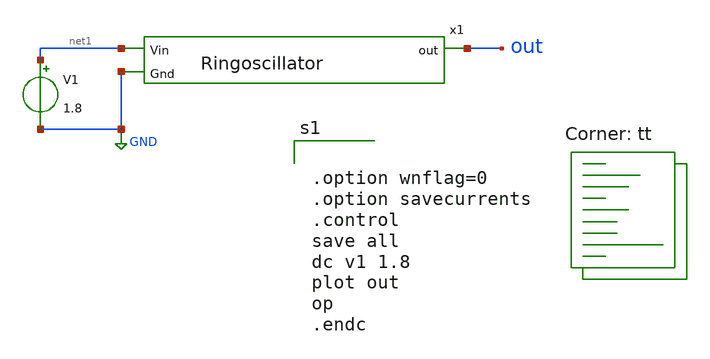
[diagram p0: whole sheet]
** sch_path: Inverter-Ringoscillator/RIngoscillator_simulation.sch
**.subckt RIngoscillator_simulation
x1 net1 out GND Ringoscillator
V1 net1 GND 1.8
**** begin user architecture code


.option wnflag=0
.option savecurrents
.control
save all
dc v1 1.8
plot out
op
.endc


.lib $::SKYWATER_MODELS/sky130.lib.spice tt
**** end user architecture code
**.ends

* expanding   symbol:  Ringoscillator.sym # of pins=3
** sym_path: Inverter-Ringoscillator/Ringoscillator.sym
** sch_path: Inverter-Ringoscillator/Ringoscillator.sch
.subckt Ringoscillator Vin out Gnd
*.opin out
*.ipin Vin
*.ipin Gnd
x1 Vin out net1 Gnd inverter
x2 Vin net1 net2 Gnd inverter
x3 Vin net2 out Gnd inverter
.ends


* expanding   symbol:  inverter.sym # of pins=4
** sym_path: Inverter-Ringoscillator/inverter.sym
** sch_path: Inverter-Ringoscillator/inverter.sch
.subckt inverter Vin in out Gnd
*.ipin in
*.ipin Vin
*.ipin Gnd
*.opin out
XM1 out in Gnd Gnd sky130_fd_pr__nfet_01v8 L=0.15 W=1 nf=1 ad='int((nf+1)/2) * W/nf * 0.29' as='int((nf+2)/2) * W/nf * 0.29'
+ pd='2*int((nf+1)/2) * (W/nf + 0.29)' ps='2*int((nf+2)/2) * (W/nf + 0.29)' nrd='0.29 / W' nrs='0.29 / W'
+ sa=0 sb=0 sd=0 mult=1 m=1
XM2 out in Vin Vin sky130_fd_pr__pfet_01v8 L=0.15 W=1 nf=1 ad='int((nf+1)/2) * W/nf * 0.29' as='int((nf+2)/2) * W/nf * 0.29'
+ pd='2*int((nf+1)/2) * (W/nf + 0.29)' ps='2*int((nf+2)/2) * (W/nf + 0.29)' nrd='0.29 / W' nrs='0.29 / W'
+ sa=0 sb=0 sd=0 mult=1 m=1
.ends

.GLOBAL GND
.end
